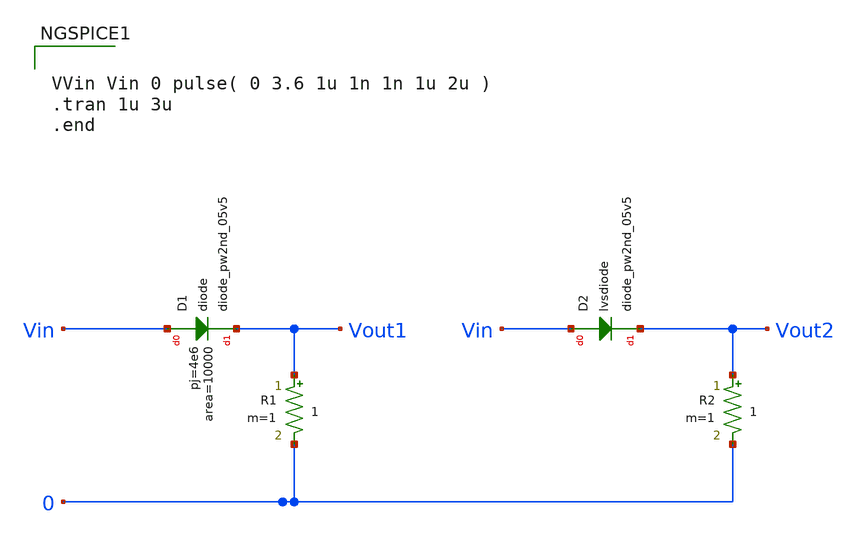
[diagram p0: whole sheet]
** sch_path: testing/test_diode.sch
**.subckt test_diode
XD1 Vin Vout1 sky130_fd_pr__diode_pw2nd_05v5 area=10000 pj=4e6
R1 Vout1 0 1 m=1
D2 Vin Vout2 sky130_fd_pr__diode_pw2nd_05v5 area=10000
R2 Vout2 0 1 m=1
**** begin user architecture code


.param mc_mm_switch=0
.param mc_pr_switch=0
.include ~/mabrains/pdks/sky130A/libs.ref/sky130_fd_pr/spice/sky130_fd_pr__nfet_01v8__tt.corner.spice
.include ~/mabrains/pdks/sky130A/libs.ref/sky130_fd_pr/spice/sky130_fd_pr__nfet_01v8_lvt__tt.corner.spice
.include ~/mabrains/pdks/sky130A/libs.ref/sky130_fd_pr/spice/sky130_fd_pr__pfet_01v8__tt.corner.spice
.include ~/mabrains/pdks/sky130A/libs.ref/sky130_fd_pr/spice/sky130_fd_pr__nfet_03v3_nvt__tt.corner.spice
.include ~/mabrains/pdks/sky130A/libs.ref/sky130_fd_pr/spice/sky130_fd_pr__nfet_05v0_nvt__tt.corner.spice
.include ~/mabrains/pdks/sky130A/libs.ref/sky130_fd_pr/spice/sky130_fd_pr__esd_nfet_01v8__tt.corner.spice
.include ~/mabrains/pdks/sky130A/libs.ref/sky130_fd_pr/spice/sky130_fd_pr__pfet_01v8_lvt__tt.corner.spice
.include ~/mabrains/pdks/sky130A/libs.ref/sky130_fd_pr/spice/sky130_fd_pr__pfet_01v8_hvt__tt.corner.spice
.include ~/mabrains/pdks/sky130A/libs.ref/sky130_fd_pr/spice/sky130_fd_pr__esd_pfet_g5v0d10v5__tt.corner.spice
.include ~/mabrains/pdks/sky130A/libs.ref/sky130_fd_pr/spice/sky130_fd_pr__pfet_g5v0d10v5__tt.corner.spice
.include ~/mabrains/pdks/sky130A/libs.ref/sky130_fd_pr/spice/sky130_fd_pr__pfet_g5v0d16v0__tt.corner.spice
.include ~/mabrains/pdks/sky130A/libs.ref/sky130_fd_pr/spice/sky130_fd_pr__nfet_g5v0d10v5__tt.corner.spice
.include ~/mabrains/pdks/sky130A/libs.ref/sky130_fd_pr/spice/sky130_fd_pr__nfet_g5v0d16v0__tt_discrete.corner.spice
.include ~/mabrains/pdks/sky130A/libs.ref/sky130_fd_pr/spice/sky130_fd_pr__esd_nfet_g5v0d10v5__tt.corner.spice
.include ~/mabrains/pdks/sky130A/libs.tech/ngspice/corners/tt/nonfet.spice
* Mismatch parameters
.include ~/mabrains/pdks/sky130A/libs.ref/sky130_fd_pr/spice/sky130_fd_pr__nfet_01v8__mismatch.corner.spice
.include ~/mabrains/pdks/sky130A/libs.ref/sky130_fd_pr/spice/sky130_fd_pr__pfet_01v8__mismatch.corner.spice
.include ~/mabrains/pdks/sky130A/libs.ref/sky130_fd_pr/spice/sky130_fd_pr__nfet_01v8_lvt__mismatch.corner.spice
.include ~/mabrains/pdks/sky130A/libs.ref/sky130_fd_pr/spice/sky130_fd_pr__pfet_01v8_lvt__mismatch.corner.spice
.include ~/mabrains/pdks/sky130A/libs.ref/sky130_fd_pr/spice/sky130_fd_pr__pfet_01v8_hvt__mismatch.corner.spice
.include ~/mabrains/pdks/sky130A/libs.ref/sky130_fd_pr/spice/sky130_fd_pr__nfet_g5v0d10v5__mismatch.corner.spice
.include ~/mabrains/pdks/sky130A/libs.ref/sky130_fd_pr/spice/sky130_fd_pr__pfet_g5v0d10v5__mismatch.corner.spice
.include ~/mabrains/pdks/sky130A/libs.ref/sky130_fd_pr/spice/sky130_fd_pr__nfet_05v0_nvt__mismatch.corner.spice
.include ~/mabrains/pdks/sky130A/libs.ref/sky130_fd_pr/spice/sky130_fd_pr__nfet_03v3_nvt__mismatch.corner.spice
* Resistor/Capacitor
.include ~/mabrains/pdks/sky130A/libs.tech/ngspice/r+c/res_typical__cap_typical.spice
.include ~/mabrains/pdks/sky130A/libs.tech/ngspice/r+c/res_typical__cap_typical__lin.spice
* Special cells
.include ~/mabrains/pdks/sky130A/libs.tech/ngspice/corners/tt/specialized_cells.spice
* All models
.include ~/mabrains/pdks/sky130A/libs.tech/ngspice/all.spice
* Corner
.include ~/mabrains/pdks/sky130A/libs.tech/ngspice/corners/tt/rf.spice





VVin Vin 0 pulse( 0 3.6 1u 1n 1n 1u 2u )
.tran 1u 3u
.end


**** end user architecture code
**.ends
.end
